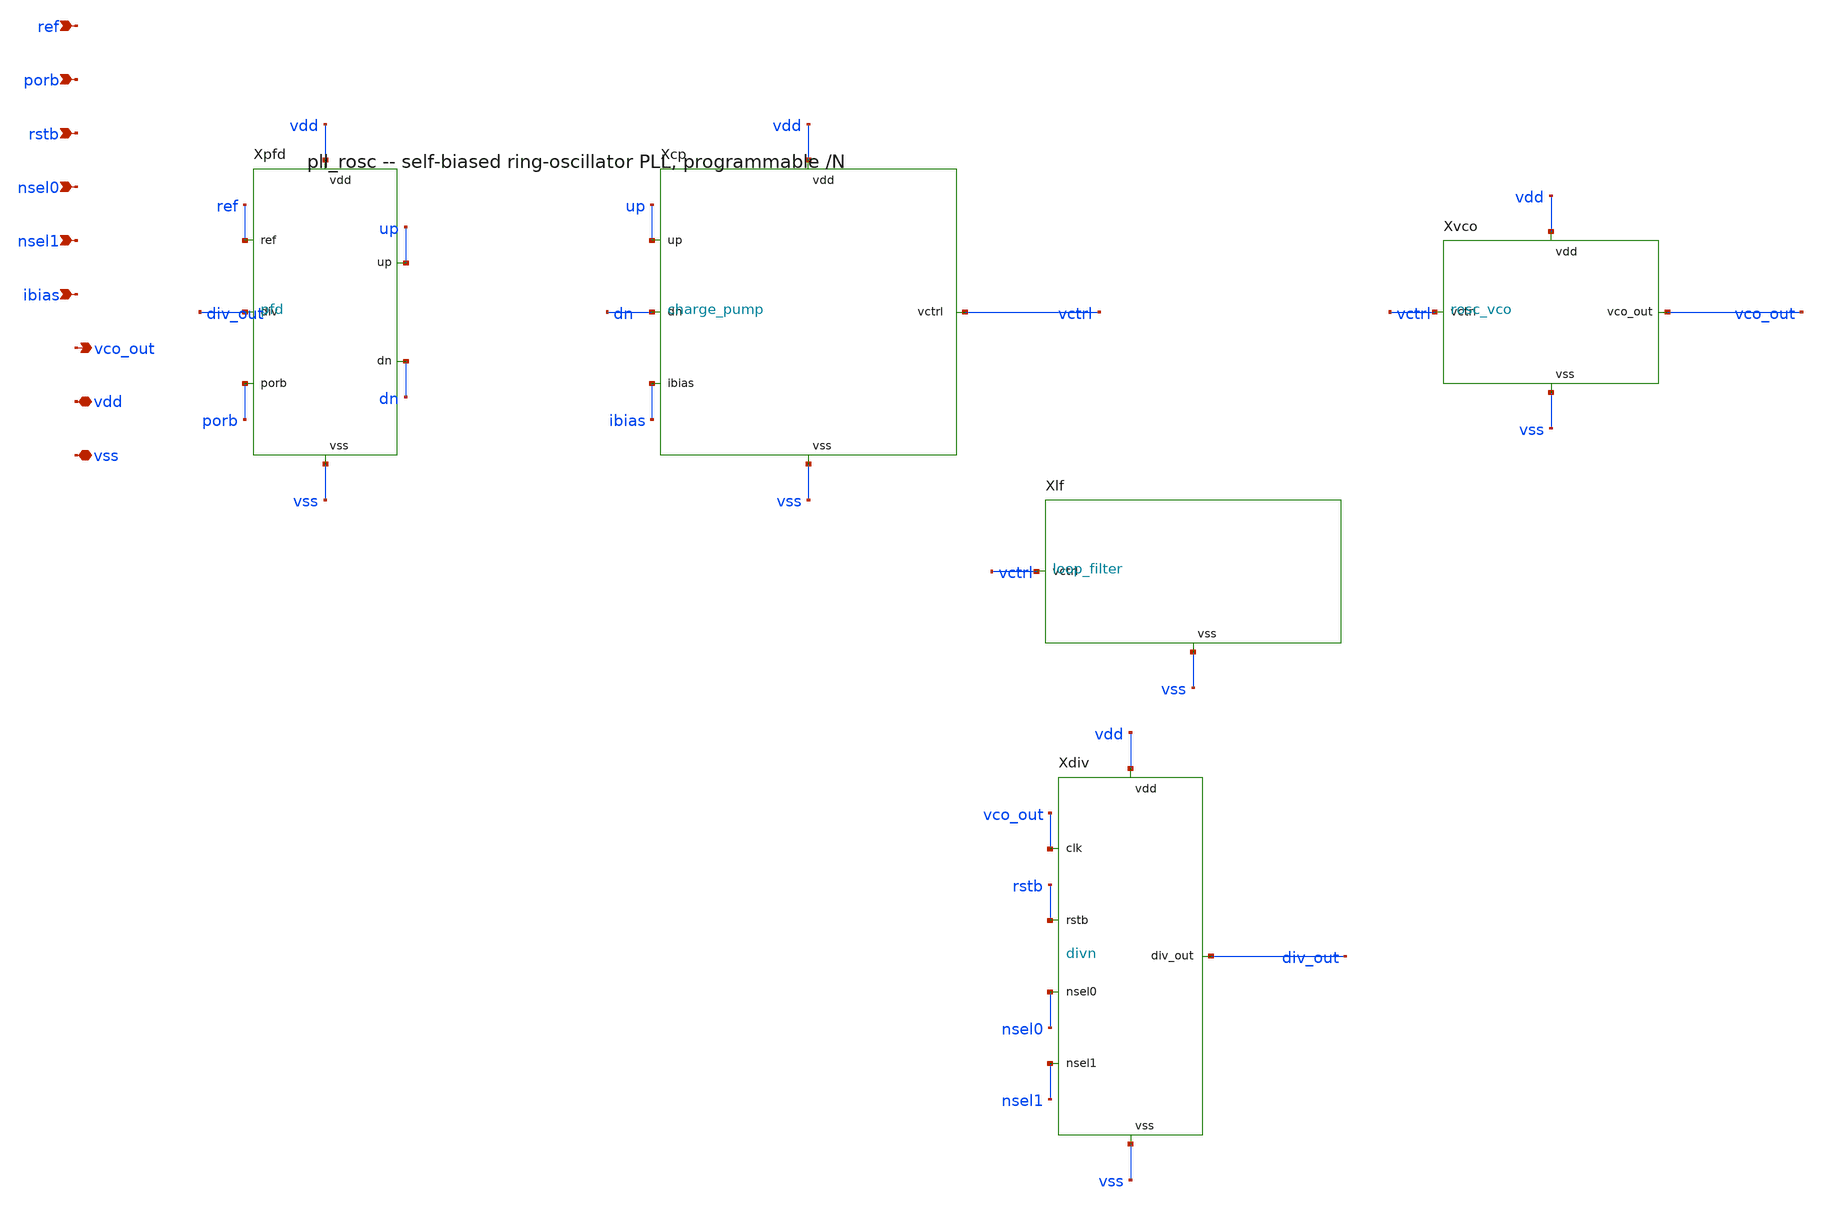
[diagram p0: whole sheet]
** sch_path: xschem/pll_rosc.sch
**.subckt pll_rosc ref porb rstb nsel0 nsel1 ibias vco_out vdd vss
*.ipin ref
*.ipin porb
*.ipin rstb
*.ipin nsel0
*.ipin nsel1
*.ipin ibias
*.opin vco_out
*.iopin vdd
*.iopin vss
Xpfd ref div_out porb up dn vdd vss pfd
Xcp up dn ibias vctrl vdd vss charge_pump
Xlf vctrl vss loop_filter
Xvco vctrl vco_out vdd vss rosc_vco
Xdiv vco_out rstb nsel0 nsel1 div_out vdd vss divn
**.ends
.end
